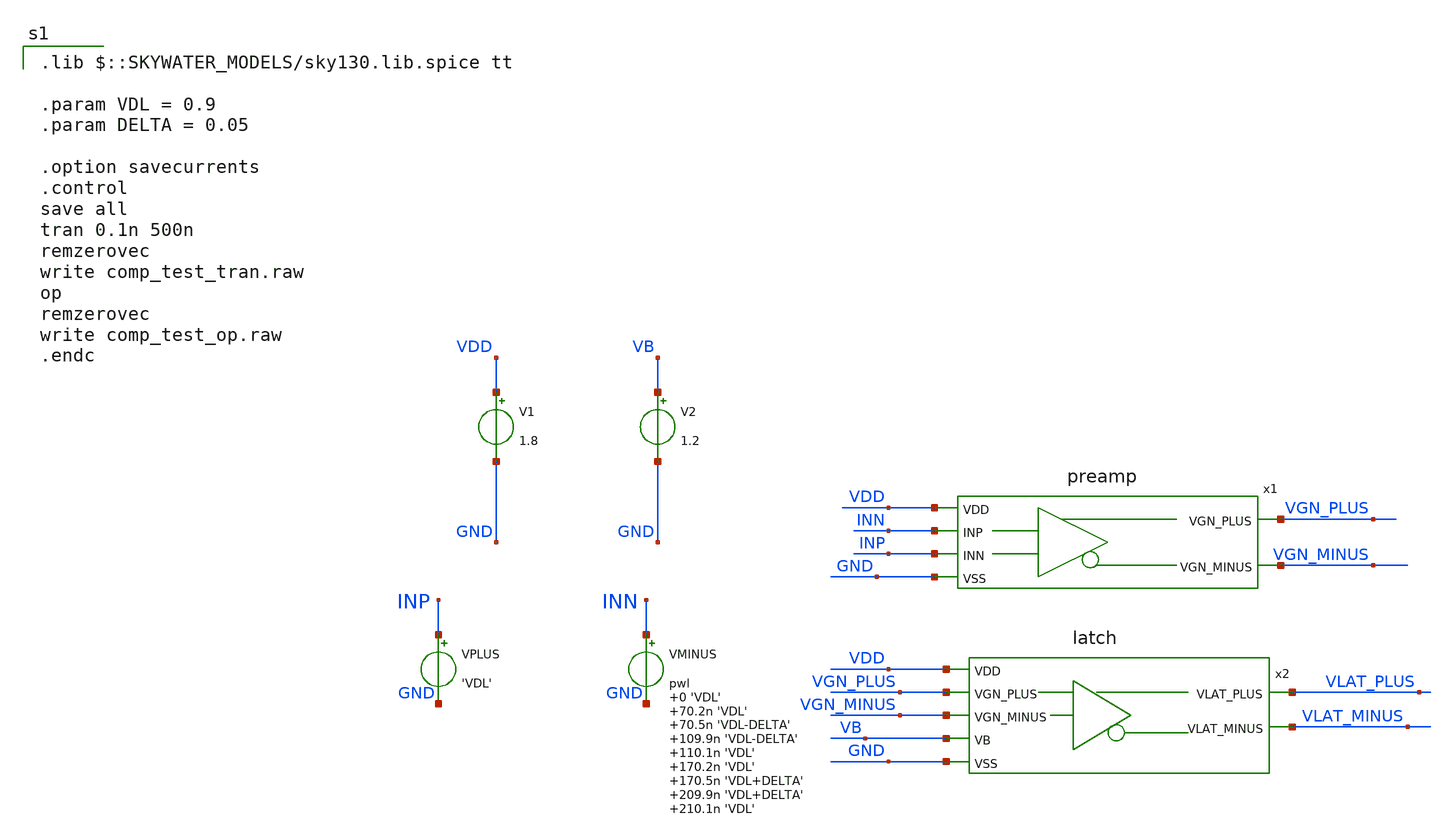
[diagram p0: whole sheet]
** sch_path: high_speed_comp_test.sch
**.subckt high_speed_comp_test
V1 VDD GND 1.8
VPLUS INP GND 'VDL'
VMINUS INN GND pwl 0 'VDL' 70.2n 'VDL' 70.5n 'VDL-DELTA' 109.9n 'VDL-DELTA' 110.1n 'VDL' 170.2n 'VDL'
+ 170.5n 'VDL+DELTA' 209.9n 'VDL+DELTA' 210.1n 'VDL'
x1 VDD VGN_PLUS VGN_MINUS INN INP GND preamp
x2 VDD VLAT_PLUS VLAT_MINUS VGN_PLUS VGN_MINUS VB GND latch
V2 VB GND 1.2
**** begin user architecture code
 .lib $::SKYWATER_MODELS/sky130.lib.spice tt

.param VDL = 0.9
.param DELTA = 0.05

.option savecurrents
.control
save all
tran 0.1n 500n
remzerovec
write comp_test_tran.raw
op
remzerovec
write comp_test_op.raw
.endc



**** end user architecture code
**.ends
.end
